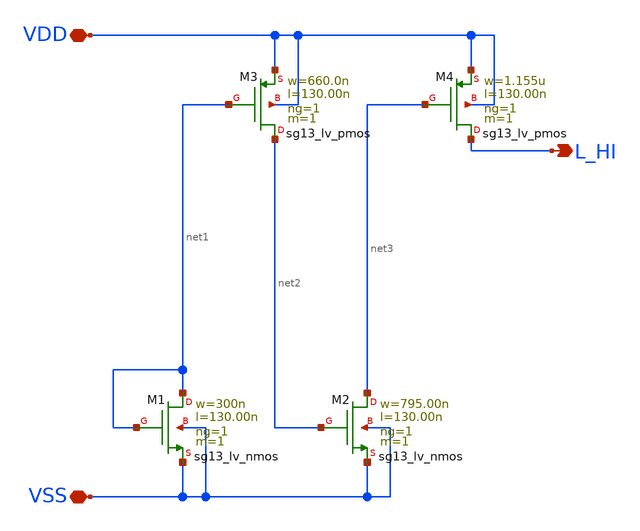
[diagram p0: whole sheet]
** sch_path: ihp-sg13g2/libs.tech/xschem/sg13g2_stdcells/sg13g2_tiehi.sch
**.subckt sg13g2_tiehi L_HI VDD VSS
*.opin L_HI
*.iopin VDD
*.iopin VSS
XM1 net1 net1 VSS VSS sg13_lv_nmos w=300n l=130.00n ng=1 m=1 mm_ok=1
XM2 net3 net2 VSS VSS sg13_lv_nmos w=795.00n l=130.00n ng=1 m=1 mm_ok=1
XM3 net2 net1 VDD VDD sg13_lv_pmos w=660.0n l=130.00n ng=1 m=1 mm_ok=1
XM4 L_HI net3 VDD VDD sg13_lv_pmos w=1.155u l=130.00n ng=1 m=1 mm_ok=1
**.ends
.end
